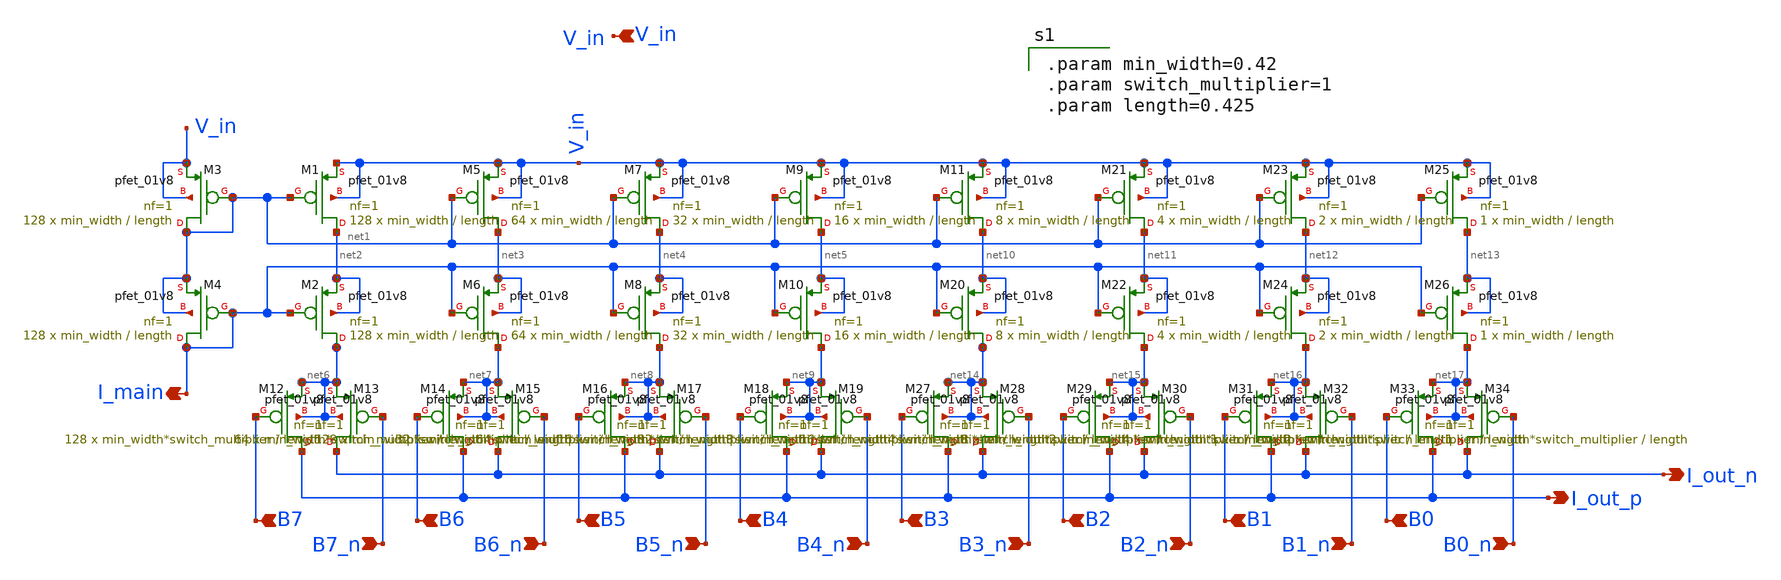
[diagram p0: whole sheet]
** sch_path: analog/schematics/components/DAC/DAC.sch
**.subckt DAC B0 B0_n B1 B2 B3 B1_n B2_n B3_n B4 B4_n B5 B6 B7 B5_n B6_n B7_n I_out_p V_in I_out_n
*+ I_main
*.ipin B0
*.ipin B0_n
*.ipin B1
*.ipin B2
*.ipin B3
*.ipin B1_n
*.ipin B2_n
*.ipin B3_n
*.ipin B4
*.ipin B4_n
*.ipin B5
*.ipin B6
*.ipin B7
*.ipin B5_n
*.ipin B6_n
*.ipin B7_n
*.opin I_out_p
*.ipin V_in
*.opin I_out_n
*.opin I_main
XM1 net2 net1 V_in V_in sky130_fd_pr__pfet_01v8 L=length W=min_width nf=1 ad='int((nf+1)/2) * W/nf * 0.29'
+ as='int((nf+2)/2) * W/nf * 0.29' pd='2*int((nf+1)/2) * (W/nf + 0.29)' ps='2*int((nf+2)/2) * (W/nf + 0.29)'
+ nrd='0.29 / W' nrs='0.29 / W' sa=0 sb=0 sd=0 mult=128 m=128
XM2 net6 I_main net2 net2 sky130_fd_pr__pfet_01v8 L=length W=min_width nf=1 ad='int((nf+1)/2) * W/nf * 0.29'
+ as='int((nf+2)/2) * W/nf * 0.29' pd='2*int((nf+1)/2) * (W/nf + 0.29)' ps='2*int((nf+2)/2) * (W/nf + 0.29)'
+ nrd='0.29 / W' nrs='0.29 / W' sa=0 sb=0 sd=0 mult=128 m=128
XM3 net1 net1 V_in V_in sky130_fd_pr__pfet_01v8 L=length W=min_width nf=1 ad='int((nf+1)/2) * W/nf * 0.29'
+ as='int((nf+2)/2) * W/nf * 0.29' pd='2*int((nf+1)/2) * (W/nf + 0.29)' ps='2*int((nf+2)/2) * (W/nf + 0.29)'
+ nrd='0.29 / W' nrs='0.29 / W' sa=0 sb=0 sd=0 mult=128 m=128
XM4 I_main I_main net1 net1 sky130_fd_pr__pfet_01v8 L=length W=min_width nf=1 ad='int((nf+1)/2) * W/nf * 0.29'
+ as='int((nf+2)/2) * W/nf * 0.29' pd='2*int((nf+1)/2) * (W/nf + 0.29)' ps='2*int((nf+2)/2) * (W/nf + 0.29)'
+ nrd='0.29 / W' nrs='0.29 / W' sa=0 sb=0 sd=0 mult=128 m=128
XM5 net3 net1 V_in V_in sky130_fd_pr__pfet_01v8 L=length W=min_width nf=1 ad='int((nf+1)/2) * W/nf * 0.29'
+ as='int((nf+2)/2) * W/nf * 0.29' pd='2*int((nf+1)/2) * (W/nf + 0.29)' ps='2*int((nf+2)/2) * (W/nf + 0.29)'
+ nrd='0.29 / W' nrs='0.29 / W' sa=0 sb=0 sd=0 mult=64 m=64
XM6 net7 I_main net3 net3 sky130_fd_pr__pfet_01v8 L=length W=min_width nf=1 ad='int((nf+1)/2) * W/nf * 0.29'
+ as='int((nf+2)/2) * W/nf * 0.29' pd='2*int((nf+1)/2) * (W/nf + 0.29)' ps='2*int((nf+2)/2) * (W/nf + 0.29)'
+ nrd='0.29 / W' nrs='0.29 / W' sa=0 sb=0 sd=0 mult=64 m=64
XM7 net4 net1 V_in V_in sky130_fd_pr__pfet_01v8 L=length W=min_width nf=1 ad='int((nf+1)/2) * W/nf * 0.29'
+ as='int((nf+2)/2) * W/nf * 0.29' pd='2*int((nf+1)/2) * (W/nf + 0.29)' ps='2*int((nf+2)/2) * (W/nf + 0.29)'
+ nrd='0.29 / W' nrs='0.29 / W' sa=0 sb=0 sd=0 mult=32 m=32
XM8 net8 I_main net4 net4 sky130_fd_pr__pfet_01v8 L=length W=min_width nf=1 ad='int((nf+1)/2) * W/nf * 0.29'
+ as='int((nf+2)/2) * W/nf * 0.29' pd='2*int((nf+1)/2) * (W/nf + 0.29)' ps='2*int((nf+2)/2) * (W/nf + 0.29)'
+ nrd='0.29 / W' nrs='0.29 / W' sa=0 sb=0 sd=0 mult=32 m=32
XM9 net5 net1 V_in V_in sky130_fd_pr__pfet_01v8 L=length W=min_width nf=1 ad='int((nf+1)/2) * W/nf * 0.29'
+ as='int((nf+2)/2) * W/nf * 0.29' pd='2*int((nf+1)/2) * (W/nf + 0.29)' ps='2*int((nf+2)/2) * (W/nf + 0.29)'
+ nrd='0.29 / W' nrs='0.29 / W' sa=0 sb=0 sd=0 mult=16 m=16
XM10 net9 I_main net5 net5 sky130_fd_pr__pfet_01v8 L=length W=min_width nf=1 ad='int((nf+1)/2) * W/nf * 0.29'
+ as='int((nf+2)/2) * W/nf * 0.29' pd='2*int((nf+1)/2) * (W/nf + 0.29)' ps='2*int((nf+2)/2) * (W/nf + 0.29)'
+ nrd='0.29 / W' nrs='0.29 / W' sa=0 sb=0 sd=0 mult=16 m=16
XM12 I_out_p B7 net6 net6 sky130_fd_pr__pfet_01v8 L=length W=min_width*switch_multiplier nf=1 ad='int((nf+1)/2) * W/nf * 0.29'
+ as='int((nf+2)/2) * W/nf * 0.29' pd='2*int((nf+1)/2) * (W/nf + 0.29)' ps='2*int((nf+2)/2) * (W/nf + 0.29)'
+ nrd='0.29 / W' nrs='0.29 / W' sa=0 sb=0 sd=0 mult=128 m=128
XM13 I_out_n B7_n net6 net6 sky130_fd_pr__pfet_01v8 L=length W=min_width*switch_multiplier nf=1 ad='int((nf+1)/2) * W/nf * 0.29'
+ as='int((nf+2)/2) * W/nf * 0.29' pd='2*int((nf+1)/2) * (W/nf + 0.29)' ps='2*int((nf+2)/2) * (W/nf + 0.29)'
+ nrd='0.29 / W' nrs='0.29 / W' sa=0 sb=0 sd=0 mult=128 m=128
XM14 I_out_p B6 net7 net7 sky130_fd_pr__pfet_01v8 L=length W=min_width*switch_multiplier nf=1 ad='int((nf+1)/2) * W/nf * 0.29'
+ as='int((nf+2)/2) * W/nf * 0.29' pd='2*int((nf+1)/2) * (W/nf + 0.29)' ps='2*int((nf+2)/2) * (W/nf + 0.29)'
+ nrd='0.29 / W' nrs='0.29 / W' sa=0 sb=0 sd=0 mult=64 m=64
XM15 I_out_n B6_n net7 net7 sky130_fd_pr__pfet_01v8 L=length W=min_width*switch_multiplier nf=1 ad='int((nf+1)/2) * W/nf * 0.29'
+ as='int((nf+2)/2) * W/nf * 0.29' pd='2*int((nf+1)/2) * (W/nf + 0.29)' ps='2*int((nf+2)/2) * (W/nf + 0.29)'
+ nrd='0.29 / W' nrs='0.29 / W' sa=0 sb=0 sd=0 mult=64 m=64
XM16 I_out_p B5 net8 net8 sky130_fd_pr__pfet_01v8 L=length W=min_width*switch_multiplier nf=1 ad='int((nf+1)/2) * W/nf * 0.29'
+ as='int((nf+2)/2) * W/nf * 0.29' pd='2*int((nf+1)/2) * (W/nf + 0.29)' ps='2*int((nf+2)/2) * (W/nf + 0.29)'
+ nrd='0.29 / W' nrs='0.29 / W' sa=0 sb=0 sd=0 mult=32 m=32
XM17 I_out_n B5_n net8 net8 sky130_fd_pr__pfet_01v8 L=length W=min_width*switch_multiplier nf=1 ad='int((nf+1)/2) * W/nf * 0.29'
+ as='int((nf+2)/2) * W/nf * 0.29' pd='2*int((nf+1)/2) * (W/nf + 0.29)' ps='2*int((nf+2)/2) * (W/nf + 0.29)'
+ nrd='0.29 / W' nrs='0.29 / W' sa=0 sb=0 sd=0 mult=32 m=32
XM18 I_out_p B4 net9 net9 sky130_fd_pr__pfet_01v8 L=length W=min_width*switch_multiplier nf=1 ad='int((nf+1)/2) * W/nf * 0.29'
+ as='int((nf+2)/2) * W/nf * 0.29' pd='2*int((nf+1)/2) * (W/nf + 0.29)' ps='2*int((nf+2)/2) * (W/nf + 0.29)'
+ nrd='0.29 / W' nrs='0.29 / W' sa=0 sb=0 sd=0 mult=16 m=16
XM19 I_out_n B4_n net9 net9 sky130_fd_pr__pfet_01v8 L=length W=min_width*switch_multiplier nf=1 ad='int((nf+1)/2) * W/nf * 0.29'
+ as='int((nf+2)/2) * W/nf * 0.29' pd='2*int((nf+1)/2) * (W/nf + 0.29)' ps='2*int((nf+2)/2) * (W/nf + 0.29)'
+ nrd='0.29 / W' nrs='0.29 / W' sa=0 sb=0 sd=0 mult=16 m=16
XM11 net10 net1 V_in V_in sky130_fd_pr__pfet_01v8 L=length W=min_width nf=1 ad='int((nf+1)/2) * W/nf * 0.29'
+ as='int((nf+2)/2) * W/nf * 0.29' pd='2*int((nf+1)/2) * (W/nf + 0.29)' ps='2*int((nf+2)/2) * (W/nf + 0.29)'
+ nrd='0.29 / W' nrs='0.29 / W' sa=0 sb=0 sd=0 mult=8 m=8
XM20 net14 I_main net10 net10 sky130_fd_pr__pfet_01v8 L=length W=min_width nf=1 ad='int((nf+1)/2) * W/nf * 0.29'
+ as='int((nf+2)/2) * W/nf * 0.29' pd='2*int((nf+1)/2) * (W/nf + 0.29)' ps='2*int((nf+2)/2) * (W/nf + 0.29)'
+ nrd='0.29 / W' nrs='0.29 / W' sa=0 sb=0 sd=0 mult=8 m=8
XM21 net11 net1 V_in V_in sky130_fd_pr__pfet_01v8 L=length W=min_width nf=1 ad='int((nf+1)/2) * W/nf * 0.29'
+ as='int((nf+2)/2) * W/nf * 0.29' pd='2*int((nf+1)/2) * (W/nf + 0.29)' ps='2*int((nf+2)/2) * (W/nf + 0.29)'
+ nrd='0.29 / W' nrs='0.29 / W' sa=0 sb=0 sd=0 mult=4 m=4
XM22 net15 I_main net11 net11 sky130_fd_pr__pfet_01v8 L=length W=min_width nf=1 ad='int((nf+1)/2) * W/nf * 0.29'
+ as='int((nf+2)/2) * W/nf * 0.29' pd='2*int((nf+1)/2) * (W/nf + 0.29)' ps='2*int((nf+2)/2) * (W/nf + 0.29)'
+ nrd='0.29 / W' nrs='0.29 / W' sa=0 sb=0 sd=0 mult=4 m=4
XM23 net12 net1 V_in V_in sky130_fd_pr__pfet_01v8 L=length W=min_width nf=1 ad='int((nf+1)/2) * W/nf * 0.29'
+ as='int((nf+2)/2) * W/nf * 0.29' pd='2*int((nf+1)/2) * (W/nf + 0.29)' ps='2*int((nf+2)/2) * (W/nf + 0.29)'
+ nrd='0.29 / W' nrs='0.29 / W' sa=0 sb=0 sd=0 mult=2 m=2
XM24 net16 I_main net12 net12 sky130_fd_pr__pfet_01v8 L=length W=min_width nf=1 ad='int((nf+1)/2) * W/nf * 0.29'
+ as='int((nf+2)/2) * W/nf * 0.29' pd='2*int((nf+1)/2) * (W/nf + 0.29)' ps='2*int((nf+2)/2) * (W/nf + 0.29)'
+ nrd='0.29 / W' nrs='0.29 / W' sa=0 sb=0 sd=0 mult=2 m=2
XM25 net13 net1 V_in V_in sky130_fd_pr__pfet_01v8 L=length W=min_width nf=1 ad='int((nf+1)/2) * W/nf * 0.29'
+ as='int((nf+2)/2) * W/nf * 0.29' pd='2*int((nf+1)/2) * (W/nf + 0.29)' ps='2*int((nf+2)/2) * (W/nf + 0.29)'
+ nrd='0.29 / W' nrs='0.29 / W' sa=0 sb=0 sd=0 mult=1 m=1
XM26 net17 I_main net13 net13 sky130_fd_pr__pfet_01v8 L=length W=min_width nf=1 ad='int((nf+1)/2) * W/nf * 0.29'
+ as='int((nf+2)/2) * W/nf * 0.29' pd='2*int((nf+1)/2) * (W/nf + 0.29)' ps='2*int((nf+2)/2) * (W/nf + 0.29)'
+ nrd='0.29 / W' nrs='0.29 / W' sa=0 sb=0 sd=0 mult=1 m=1
XM27 I_out_p B3 net14 net14 sky130_fd_pr__pfet_01v8 L=length W=min_width*switch_multiplier nf=1 ad='int((nf+1)/2) * W/nf * 0.29'
+ as='int((nf+2)/2) * W/nf * 0.29' pd='2*int((nf+1)/2) * (W/nf + 0.29)' ps='2*int((nf+2)/2) * (W/nf + 0.29)'
+ nrd='0.29 / W' nrs='0.29 / W' sa=0 sb=0 sd=0 mult=8 m=8
XM28 I_out_n B3_n net14 net14 sky130_fd_pr__pfet_01v8 L=length W=min_width*switch_multiplier nf=1 ad='int((nf+1)/2) * W/nf * 0.29'
+ as='int((nf+2)/2) * W/nf * 0.29' pd='2*int((nf+1)/2) * (W/nf + 0.29)' ps='2*int((nf+2)/2) * (W/nf + 0.29)'
+ nrd='0.29 / W' nrs='0.29 / W' sa=0 sb=0 sd=0 mult=8 m=8
XM29 I_out_p B2 net15 net15 sky130_fd_pr__pfet_01v8 L=length W=min_width*switch_multiplier nf=1 ad='int((nf+1)/2) * W/nf * 0.29'
+ as='int((nf+2)/2) * W/nf * 0.29' pd='2*int((nf+1)/2) * (W/nf + 0.29)' ps='2*int((nf+2)/2) * (W/nf + 0.29)'
+ nrd='0.29 / W' nrs='0.29 / W' sa=0 sb=0 sd=0 mult=4 m=4
XM30 I_out_n B2_n net15 net15 sky130_fd_pr__pfet_01v8 L=length W=min_width*switch_multiplier nf=1 ad='int((nf+1)/2) * W/nf * 0.29'
+ as='int((nf+2)/2) * W/nf * 0.29' pd='2*int((nf+1)/2) * (W/nf + 0.29)' ps='2*int((nf+2)/2) * (W/nf + 0.29)'
+ nrd='0.29 / W' nrs='0.29 / W' sa=0 sb=0 sd=0 mult=4 m=4
XM31 I_out_p B1 net16 net16 sky130_fd_pr__pfet_01v8 L=length W=min_width*switch_multiplier nf=1 ad='int((nf+1)/2) * W/nf * 0.29'
+ as='int((nf+2)/2) * W/nf * 0.29' pd='2*int((nf+1)/2) * (W/nf + 0.29)' ps='2*int((nf+2)/2) * (W/nf + 0.29)'
+ nrd='0.29 / W' nrs='0.29 / W' sa=0 sb=0 sd=0 mult=2 m=2
XM32 I_out_n B1_n net16 net16 sky130_fd_pr__pfet_01v8 L=length W=min_width*switch_multiplier nf=1 ad='int((nf+1)/2) * W/nf * 0.29'
+ as='int((nf+2)/2) * W/nf * 0.29' pd='2*int((nf+1)/2) * (W/nf + 0.29)' ps='2*int((nf+2)/2) * (W/nf + 0.29)'
+ nrd='0.29 / W' nrs='0.29 / W' sa=0 sb=0 sd=0 mult=2 m=2
XM33 I_out_p B0 net17 net17 sky130_fd_pr__pfet_01v8 L=length W=min_width*switch_multiplier nf=1 ad='int((nf+1)/2) * W/nf * 0.29'
+ as='int((nf+2)/2) * W/nf * 0.29' pd='2*int((nf+1)/2) * (W/nf + 0.29)' ps='2*int((nf+2)/2) * (W/nf + 0.29)'
+ nrd='0.29 / W' nrs='0.29 / W' sa=0 sb=0 sd=0 mult=1 m=1
XM34 I_out_n B0_n net17 net17 sky130_fd_pr__pfet_01v8 L=length W=min_width*switch_multiplier nf=1 ad='int((nf+1)/2) * W/nf * 0.29'
+ as='int((nf+2)/2) * W/nf * 0.29' pd='2*int((nf+1)/2) * (W/nf + 0.29)' ps='2*int((nf+2)/2) * (W/nf + 0.29)'
+ nrd='0.29 / W' nrs='0.29 / W' sa=0 sb=0 sd=0 mult=1 m=1
**** begin user architecture code

.param min_width=0.42
.param switch_multiplier=1
.param length=0.425

**** end user architecture code
**.ends
.end
